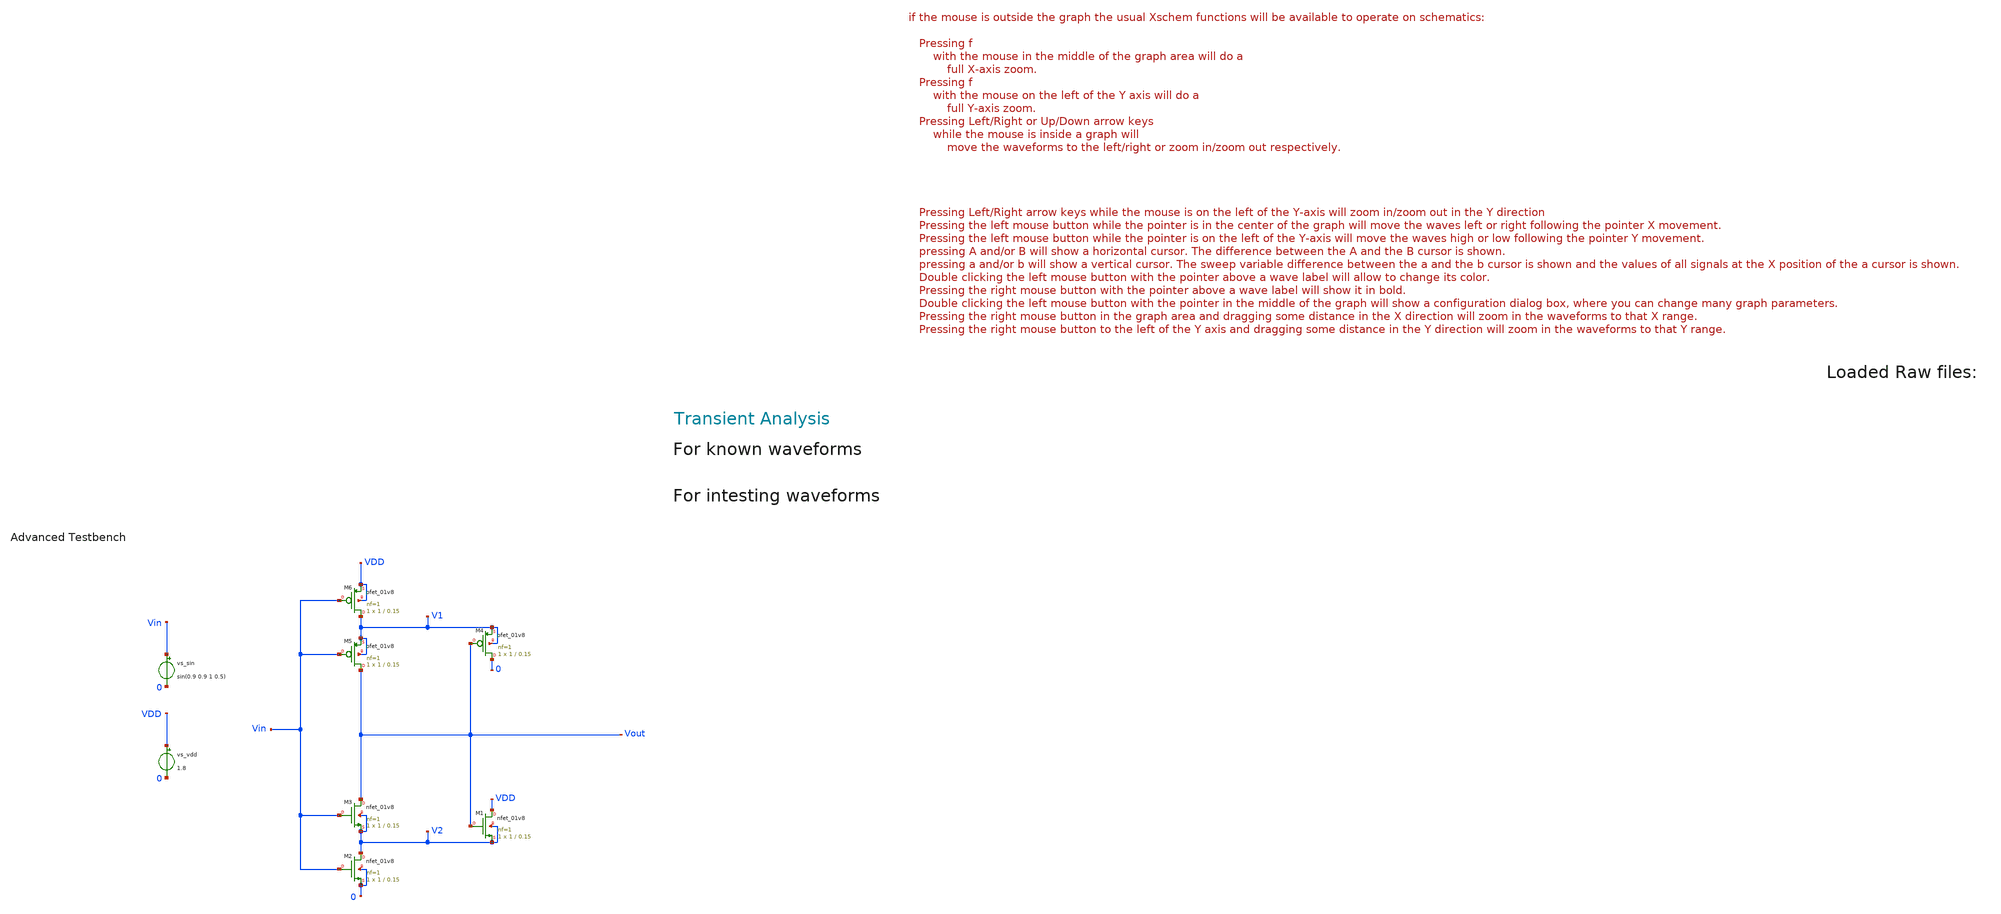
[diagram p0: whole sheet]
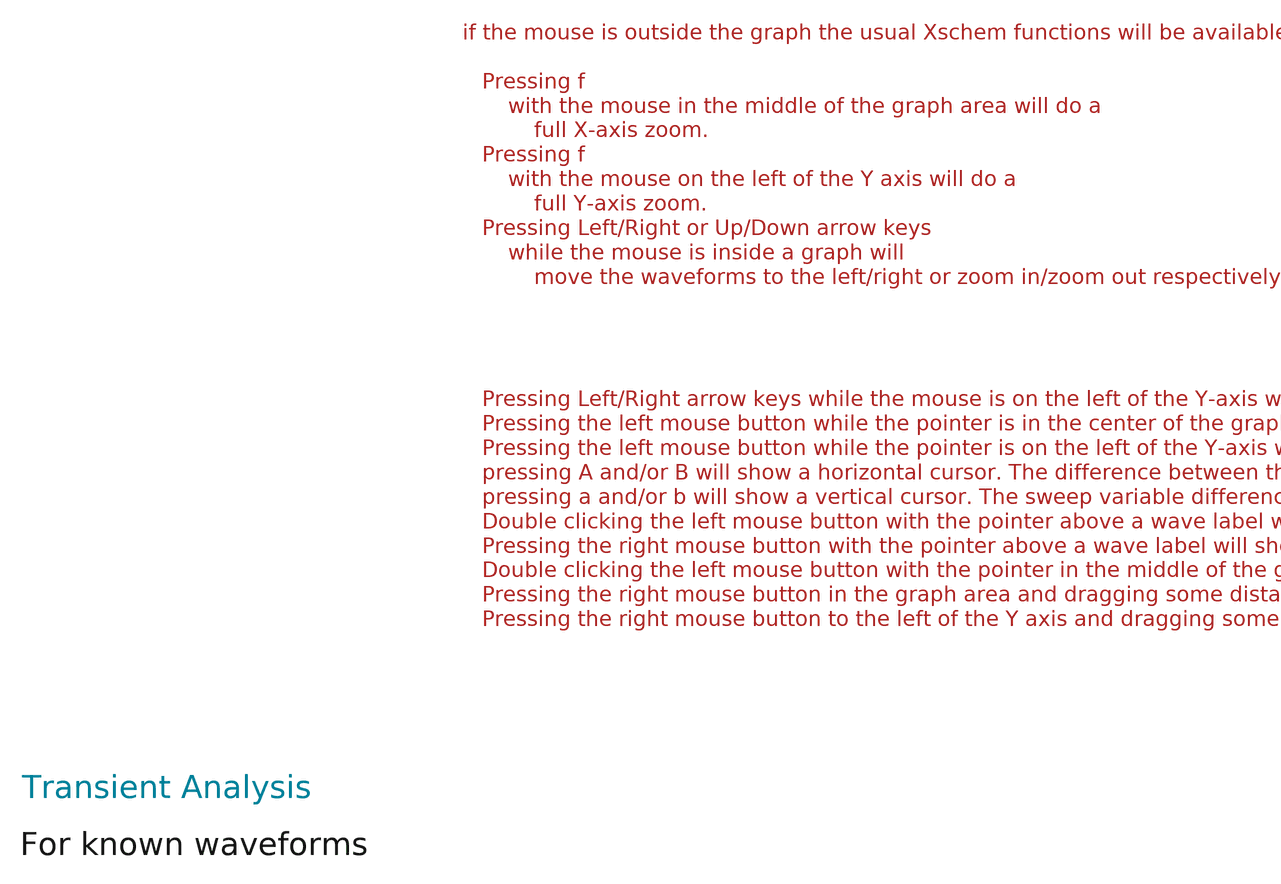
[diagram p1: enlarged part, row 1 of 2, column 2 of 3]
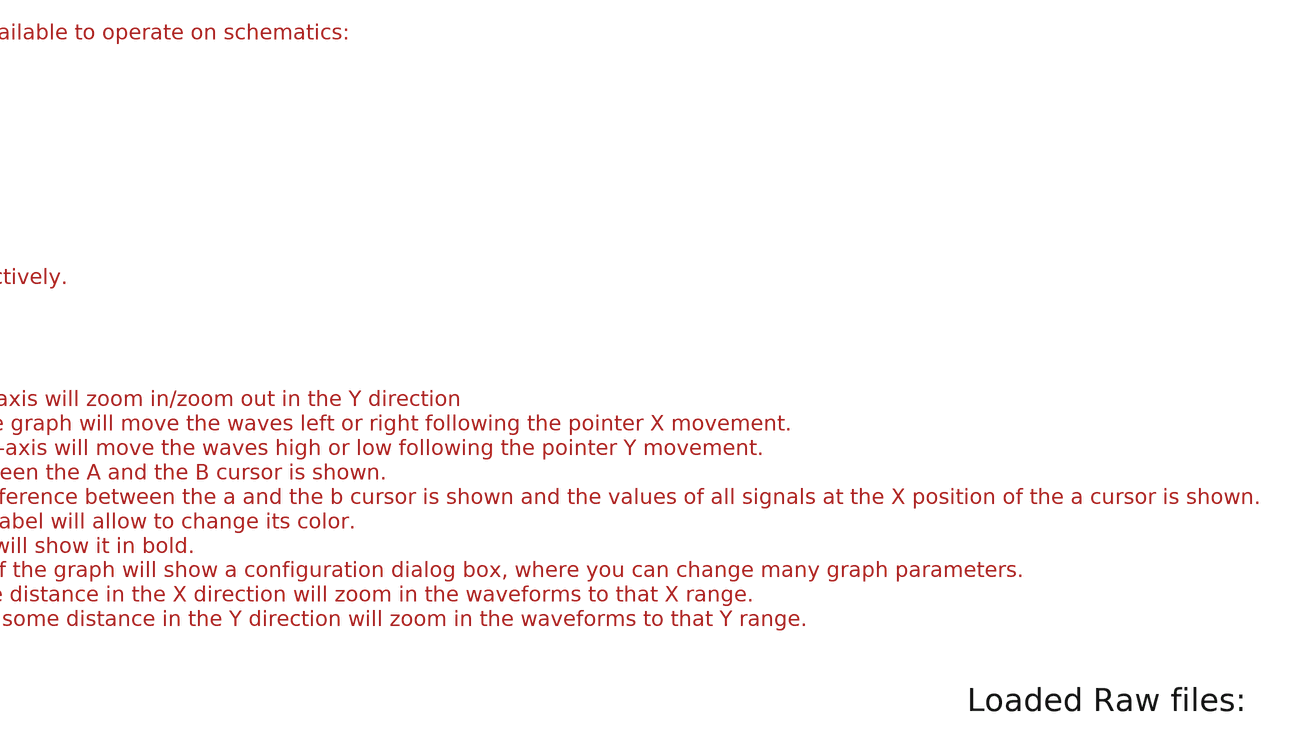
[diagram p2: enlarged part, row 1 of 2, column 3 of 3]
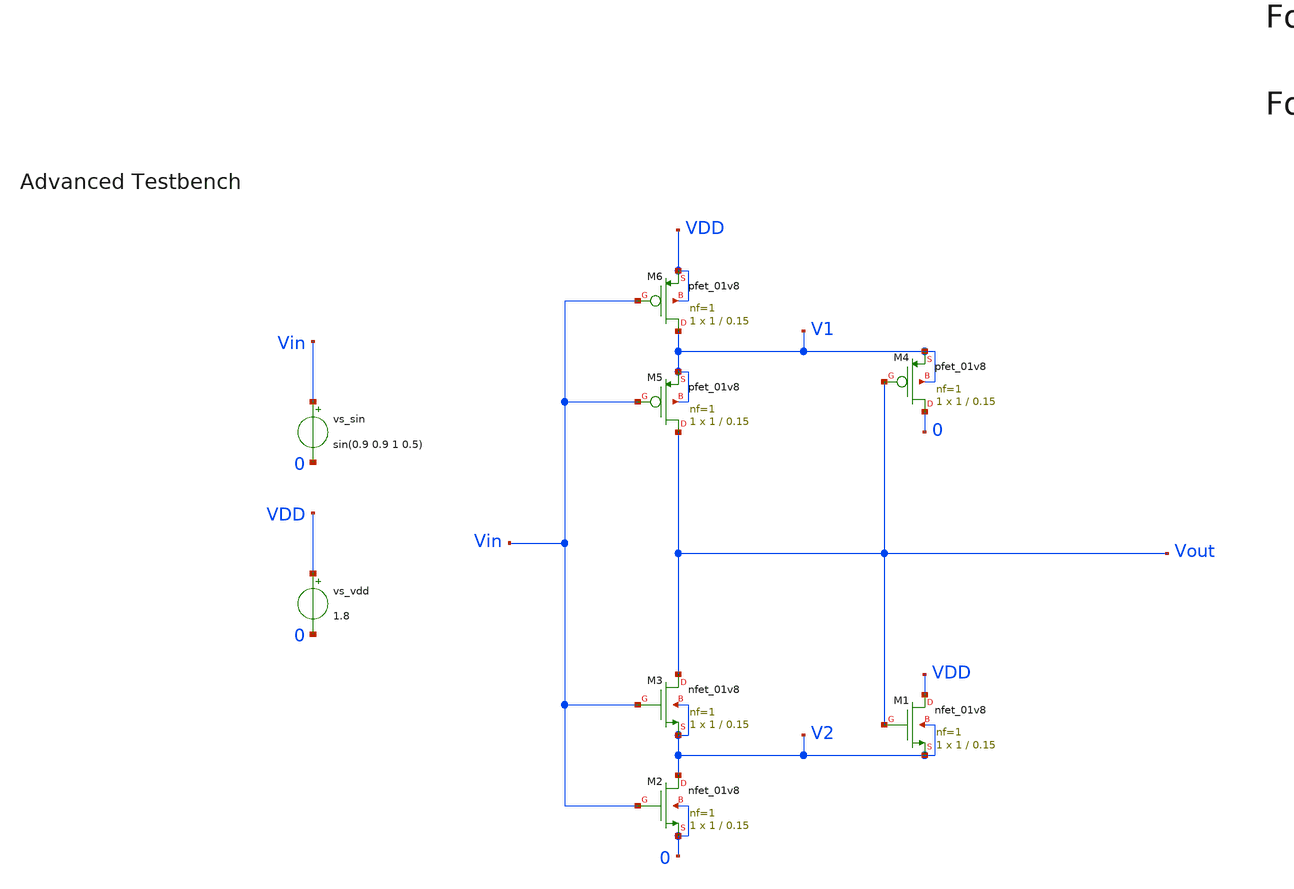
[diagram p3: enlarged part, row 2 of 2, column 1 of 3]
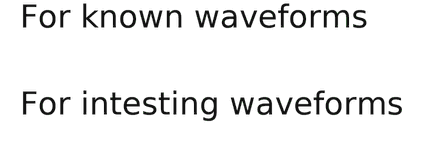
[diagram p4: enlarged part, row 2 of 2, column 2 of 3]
** sch_path: tt10-hdl/tt_um_test_commit/xschem/T1/schmTrigg_Tran-anal_tb.sch
* Copyright (C) 1998-2024 Stefan Frederik Schippers
* This program is free software; you can redistribute it and/or modify
* it under the terms of the GNU General Public License as published by
* the Free Software Foundation; either version 2 of the License, or
* (at your option) any later version.
* This program is distributed in the hope that it will be useful,
* but WITHOUT ANY WARRANTY; without even the implied warranty of
* MERCHANTABILITY or FITNESS FOR A PARTICULAR PURPOSE.  See the
* GNU General Public License for more details.
* You should have received a copy of the GNU General Public License
* along with this program; if not, write to the Free Software
**.subckt schmTrigg_Tran-anal_tb
vs_vdd VDD 0 1.8
vs_sin Vin 0 sin(0.9 0.9 1 0.5)
XM1 VDD Vout V2 V2 sky130_fd_pr__nfet_01v8 L=0.15 W=1 nf=1 ad='int((1 + 1)/2) * 1 / 1 * 0.29' as='int((1 + 2)/2) * 1 / 1 * 0.29'
+ pd='2*int((1 + 1)/2) * (1 / 1 + 0.29)' ps='2*int((1 + 2)/2) * (1 / 1 + 0.29)' nrd='0.29 / 1 ' nrs='0.29 / 1 '
+ sa=0 sb=0 sd=0 mult=1 m=1
XM2 V2 Vin 0 0 sky130_fd_pr__nfet_01v8 L=0.15 W=1 nf=1 ad='int((1 + 1)/2) * 1 / 1 * 0.29' as='int((1 + 2)/2) * 1 / 1 * 0.29'
+ pd='2*int((1 + 1)/2) * (1 / 1 + 0.29)' ps='2*int((1 + 2)/2) * (1 / 1 + 0.29)' nrd='0.29 / 1 ' nrs='0.29 / 1 '
+ sa=0 sb=0 sd=0 mult=1 m=1
XM3 Vout Vin V2 V2 sky130_fd_pr__nfet_01v8 L=0.15 W=1 nf=1 ad='int((1 + 1)/2) * 1 / 1 * 0.29' as='int((1 + 2)/2) * 1 / 1 * 0.29'
+ pd='2*int((1 + 1)/2) * (1 / 1 + 0.29)' ps='2*int((1 + 2)/2) * (1 / 1 + 0.29)' nrd='0.29 / 1 ' nrs='0.29 / 1 '
+ sa=0 sb=0 sd=0 mult=1 m=1
XM4 0 Vout V1 V1 sky130_fd_pr__pfet_01v8 L=0.15 W=1 nf=1 ad='int((nf+1)/2) * W/nf * 0.29' as='int((nf+2)/2) * W/nf * 0.29'
+ pd='2*int((nf+1)/2) * (W/nf + 0.29)' ps='2*int((nf+2)/2) * (W/nf + 0.29)' nrd='0.29 / W' nrs='0.29 / W'
+ sa=0 sb=0 sd=0 mult=1 m=1
XM5 Vout Vin V1 V1 sky130_fd_pr__pfet_01v8 L=0.15 W=1 nf=1 ad='int((nf+1)/2) * W/nf * 0.29' as='int((nf+2)/2) * W/nf * 0.29'
+ pd='2*int((nf+1)/2) * (W/nf + 0.29)' ps='2*int((nf+2)/2) * (W/nf + 0.29)' nrd='0.29 / W' nrs='0.29 / W'
+ sa=0 sb=0 sd=0 mult=1 m=1
XM6 V1 Vin VDD VDD sky130_fd_pr__pfet_01v8 L=0.15 W=1 nf=1 ad='int((nf+1)/2) * W/nf * 0.29' as='int((nf+2)/2) * W/nf * 0.29'
+ pd='2*int((nf+1)/2) * (W/nf + 0.29)' ps='2*int((nf+2)/2) * (W/nf + 0.29)' nrd='0.29 / W' nrs='0.29 / W'
+ sa=0 sb=0 sd=0 mult=1 m=1
**** begin user architecture code



.temp 30

.option savecurrents
.save all *@m1[gm]
.control
  save all alli
  op
  remzerovec
  write schmTriggTran.raw
  set appendwrite

  tran 1m 2
  remzerovec
  write schmTriggTran.raw




  *quit 0




.endc





** opencircuitdesign pdks install
.lib $::SKYWATER_MODELS/sky130.lib.spice tt
.include $::SKYWATER_STDCELLS/sky130_fd_sc_hd.spice


**** end user architecture code
**.ends
.end
